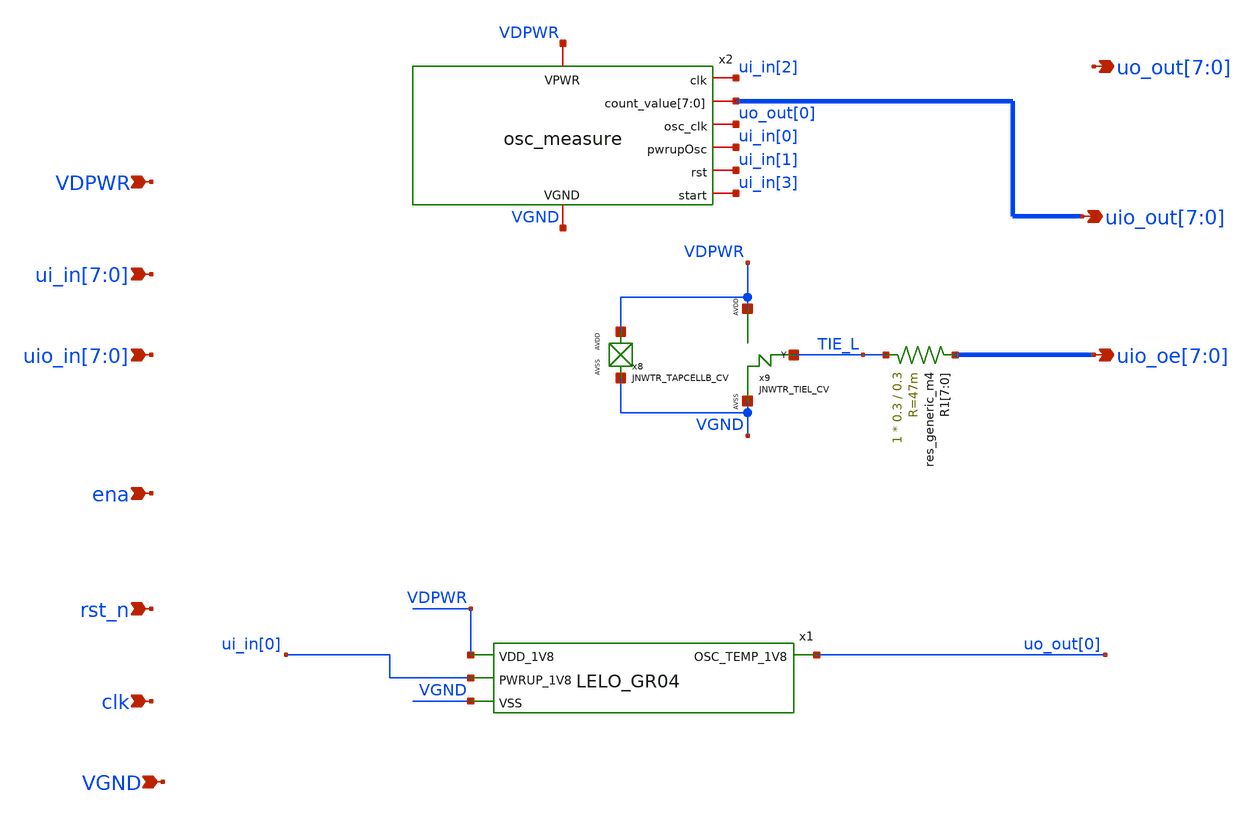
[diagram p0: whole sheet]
** sch_path: design/LELO_GR04_SKY130A/tt_um_lelo_gr04_analogicus.sch
**.subckt tt_um_lelo_gr04_analogicus
*+ uo_out[7],uo_out[6],uo_out[5],uo_out[4],uo_out[3],uo_out[2],uo_out[1],uo_out[0] uio_out[7],uio_out[6],uio_out[5],uio_out[4],uio_out[3],uio_out[2],uio_out[1],uio_out[0]
*+ uio_oe[7],uio_oe[6],uio_oe[5],uio_oe[4],uio_oe[3],uio_oe[2],uio_oe[1],uio_oe[0] VDPWR VGND ui_in[7],ui_in[6],ui_in[5],ui_in[4],ui_in[3],ui_in[2],ui_in[1],ui_in[0]
*+ uio_in[7],uio_in[6],uio_in[5],uio_in[4],uio_in[3],uio_in[2],uio_in[1],uio_in[0] ena rst_n clk
*.opin uo_out[7],uo_out[6],uo_out[5],uo_out[4],uo_out[3],uo_out[2],uo_out[1],uo_out[0]
*.opin uio_out[7],uio_out[6],uio_out[5],uio_out[4],uio_out[3],uio_out[2],uio_out[1],uio_out[0]
*.opin uio_oe[7],uio_oe[6],uio_oe[5],uio_oe[4],uio_oe[3],uio_oe[2],uio_oe[1],uio_oe[0]
*.ipin VDPWR
*.ipin VGND
*.ipin ui_in[7],ui_in[6],ui_in[5],ui_in[4],ui_in[3],ui_in[2],ui_in[1],ui_in[0]
*.ipin uio_in[7],uio_in[6],uio_in[5],uio_in[4],uio_in[3],uio_in[2],uio_in[1],uio_in[0]
*.ipin ena
*.ipin rst_n
*.ipin clk
x8 VDPWR VGND JNWTR_TAPCELLB_CV xoffset=0 yoffset=0 angle=0
R1[7] TIE_L uio_oe[7] sky130_fd_pr__res_generic_m4 W=0.3 L=0.3 m=1
R1[6] TIE_L uio_oe[6] sky130_fd_pr__res_generic_m4 W=0.3 L=0.3 m=1
R1[5] TIE_L uio_oe[5] sky130_fd_pr__res_generic_m4 W=0.3 L=0.3 m=1
R1[4] TIE_L uio_oe[4] sky130_fd_pr__res_generic_m4 W=0.3 L=0.3 m=1
R1[3] TIE_L uio_oe[3] sky130_fd_pr__res_generic_m4 W=0.3 L=0.3 m=1
R1[2] TIE_L uio_oe[2] sky130_fd_pr__res_generic_m4 W=0.3 L=0.3 m=1
R1[1] TIE_L uio_oe[1] sky130_fd_pr__res_generic_m4 W=0.3 L=0.3 m=1
R1[0] TIE_L uio_oe[0] sky130_fd_pr__res_generic_m4 W=0.3 L=0.3 m=1
x1 VDPWR uo_out[0] ui_in[0] VGND LELO_GR04
x2 ui_in[2] uo_out[0] ui_in[0] ui_in[1] ui_in[3] VDPWR VGND uio_out[7] uio_out[6] uio_out[5]
+ uio_out[4] uio_out[3] uio_out[2] uio_out[1] uio_out[0] osc_measure
**.ends
.end
